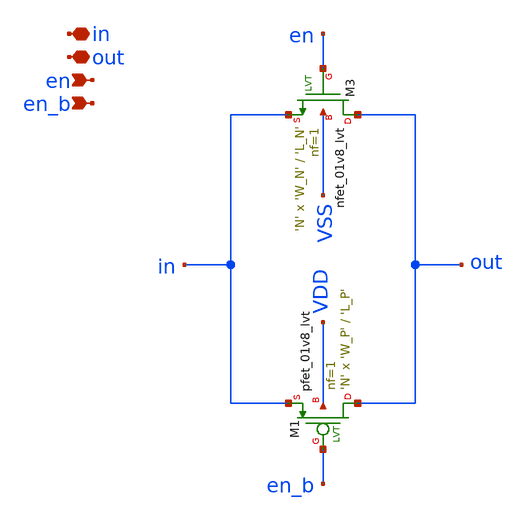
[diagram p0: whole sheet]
** sch_path: design/analog_modulator/schematic/transmission_gate_lvt.sch
**.subckt transmission_gate_lvt in out en en_b
*.iopin in
*.iopin out
*.ipin en
*.ipin en_b
XM3 out en in VSS sky130_fd_pr__nfet_01v8_lvt L='L_N' W='W_N' nf=1 ad='int((nf+1)/2) * W/nf * 0.29' as='int((nf+2)/2) * W/nf * 0.29'
+ pd='2*int((nf+1)/2) * (W/nf + 0.29)' ps='2*int((nf+2)/2) * (W/nf + 0.29)' nrd='0.29 / W' nrs='0.29 / W'
+ sa=0 sb=0 sd=0 mult='N' m='N'
XM1 out en_b in VDD sky130_fd_pr__pfet_01v8_lvt L='L_P' W='W_P' nf=1 ad='int((nf+1)/2) * W/nf * 0.29'
+ as='int((nf+2)/2) * W/nf * 0.29' pd='2*int((nf+1)/2) * (W/nf + 0.29)' ps='2*int((nf+2)/2) * (W/nf + 0.29)'
+ nrd='0.29 / W' nrs='0.29 / W' sa=0 sb=0 sd=0 mult='N' m='N'
**.ends
.end
